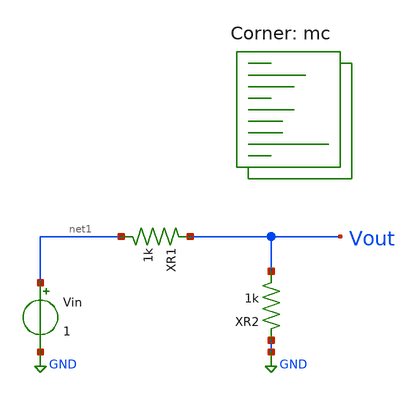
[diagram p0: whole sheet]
** sch_path: projects/montecarlo/xschem_ngspice/mcvdivider/mcvdivider.sch
**.subckt mcvdivider
Vin net1 GND 1
XR1 Vout net1 gaussres nom=1k
XR2 GND Vout gaussres nom=1k
**** begin user architecture code

.param MC_SWITCH=1.0
.subckt gaussres pos neg
.param nom=1k cv=0.005
R1 pos neg {nom + MC_SWITCH*AGAUSS(0,1,1)*cv*nom}
.ends

.option wnflag=1




.control
set wr_vecnames
set wr_singlescale

let mc_runs=10
let run=1

dowhile run <= mc_runs
  dc vin 0 1 0.01
  wrdata /foss/designs/my_design/projects/montecarlo/xschem_ngspice/mcvdivider/mcvdivider{$&run}.txt
+ v(Vout)
  reset
  let run = run + 1
end
.endc





.lib $::SKYWATER_MODELS/sky130.lib.spice mc
**** end user architecture code
**.ends
.GLOBAL GND
.end
